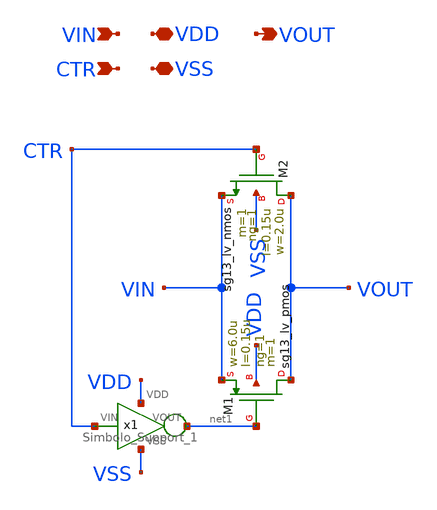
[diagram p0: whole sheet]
** sch_path: Taller2_extendido/Insumos/Transmision_Gate.sch
**.subckt Transmision_Gate VIN VDD VSS CTR VOUT
*.ipin VIN
*.iopin VDD
*.iopin VSS
*.ipin CTR
*.opin VOUT
XM1 VOUT net1 VIN VDD sg13_lv_pmos w=6.0u l=0.15u ng=1 m=1 mm_ok=1
XM2 VOUT CTR VIN VSS sg13_lv_nmos w=2.0u l=0.15u ng=1 m=1 mm_ok=1
x1 VDD CTR net1 VSS Simbolo_Support_1
**.ends

* expanding   symbol:  Simbolo_Support_1.sym # of pins=4
** sym_path: Taller2_extendido/Insumos/Simbolo_Support_1.sym
** sch_path: Taller2_extendido/Insumos/Simbolo_Support_1.sch
.subckt Simbolo_Support_1 VDD VIN VOUT VSS
*.ipin VIN
*.iopin VDD
*.iopin VSS
*.opin VOUT
XM1 VOUT VIN VDD VDD sg13_lv_pmos w=1.0u l=0.15u ng=1 m=1 mm_ok=1
XM2 VOUT VIN VSS VSS sg13_lv_nmos w=1.0u l=0.15u ng=1 m=1 mm_ok=1
.ends

.end
